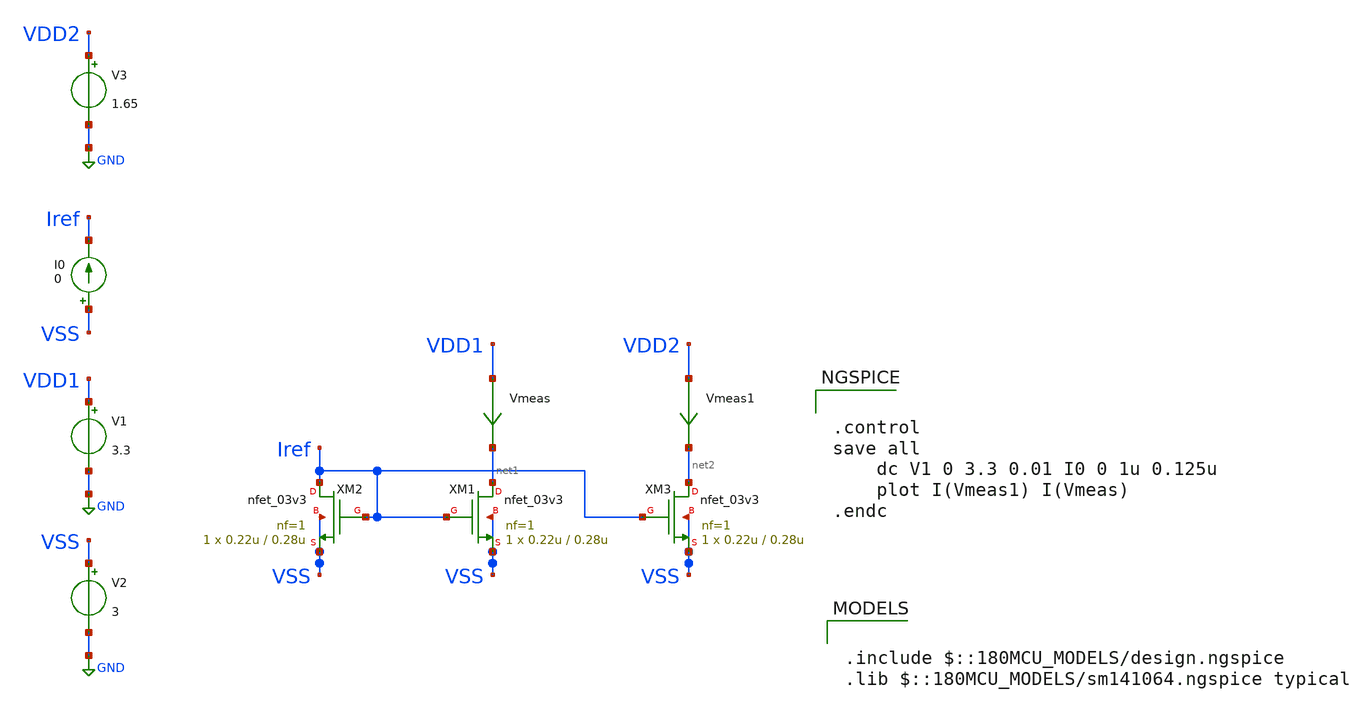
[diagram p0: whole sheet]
** sch_path: week02_current_diffpair/tugas5_cascode_current_mirror/multiple-output-current-mirror.sch
**.subckt multiple-output-current-mirror
XM1 net1 Iref VSS VSS nfet_03v3 L=0.28u W=0.22u nf=1 ad='int((nf+1)/2) * W/nf * 0.18u' as='int((nf+2)/2) * W/nf * 0.18u'
+ pd='2*int((nf+1)/2) * (W/nf + 0.18u)' ps='2*int((nf+2)/2) * (W/nf + 0.18u)' nrd='0.18u / W' nrs='0.18u / W'
+ sa=0 sb=0 sd=0 m=1
XM2 Iref Iref VSS VSS nfet_03v3 L=0.28u W=0.22u nf=1 ad='int((nf+1)/2) * W/nf * 0.18u' as='int((nf+2)/2) * W/nf * 0.18u'
+ pd='2*int((nf+1)/2) * (W/nf + 0.18u)' ps='2*int((nf+2)/2) * (W/nf + 0.18u)' nrd='0.18u / W' nrs='0.18u / W'
+ sa=0 sb=0 sd=0 m=1
I0 VSS Iref 0
XM3 net2 Iref VSS VSS nfet_03v3 L=0.28u W=0.22u nf=1 ad='int((nf+1)/2) * W/nf * 0.18u' as='int((nf+2)/2) * W/nf * 0.18u'
+ pd='2*int((nf+1)/2) * (W/nf + 0.18u)' ps='2*int((nf+2)/2) * (W/nf + 0.18u)' nrd='0.18u / W' nrs='0.18u / W'
+ sa=0 sb=0 sd=0 m=1
Vmeas VDD1 net1 0
.save i(vmeas)
Vmeas1 VDD2 net2 0
.save i(vmeas1)
V1 VDD1 GND 3.3
V2 VSS GND 3
V3 VDD2 GND 1.65
**** begin user architecture code

.include $::180MCU_MODELS/design.ngspice
.lib $::180MCU_MODELS/sm141064.ngspice typical



.control
save all
	dc V1 0 3.3 0.01 I0 0 1u 0.125u
	plot I(Vmeas1) I(Vmeas)
.endc


**** end user architecture code
**.ends
.GLOBAL GND
.end
